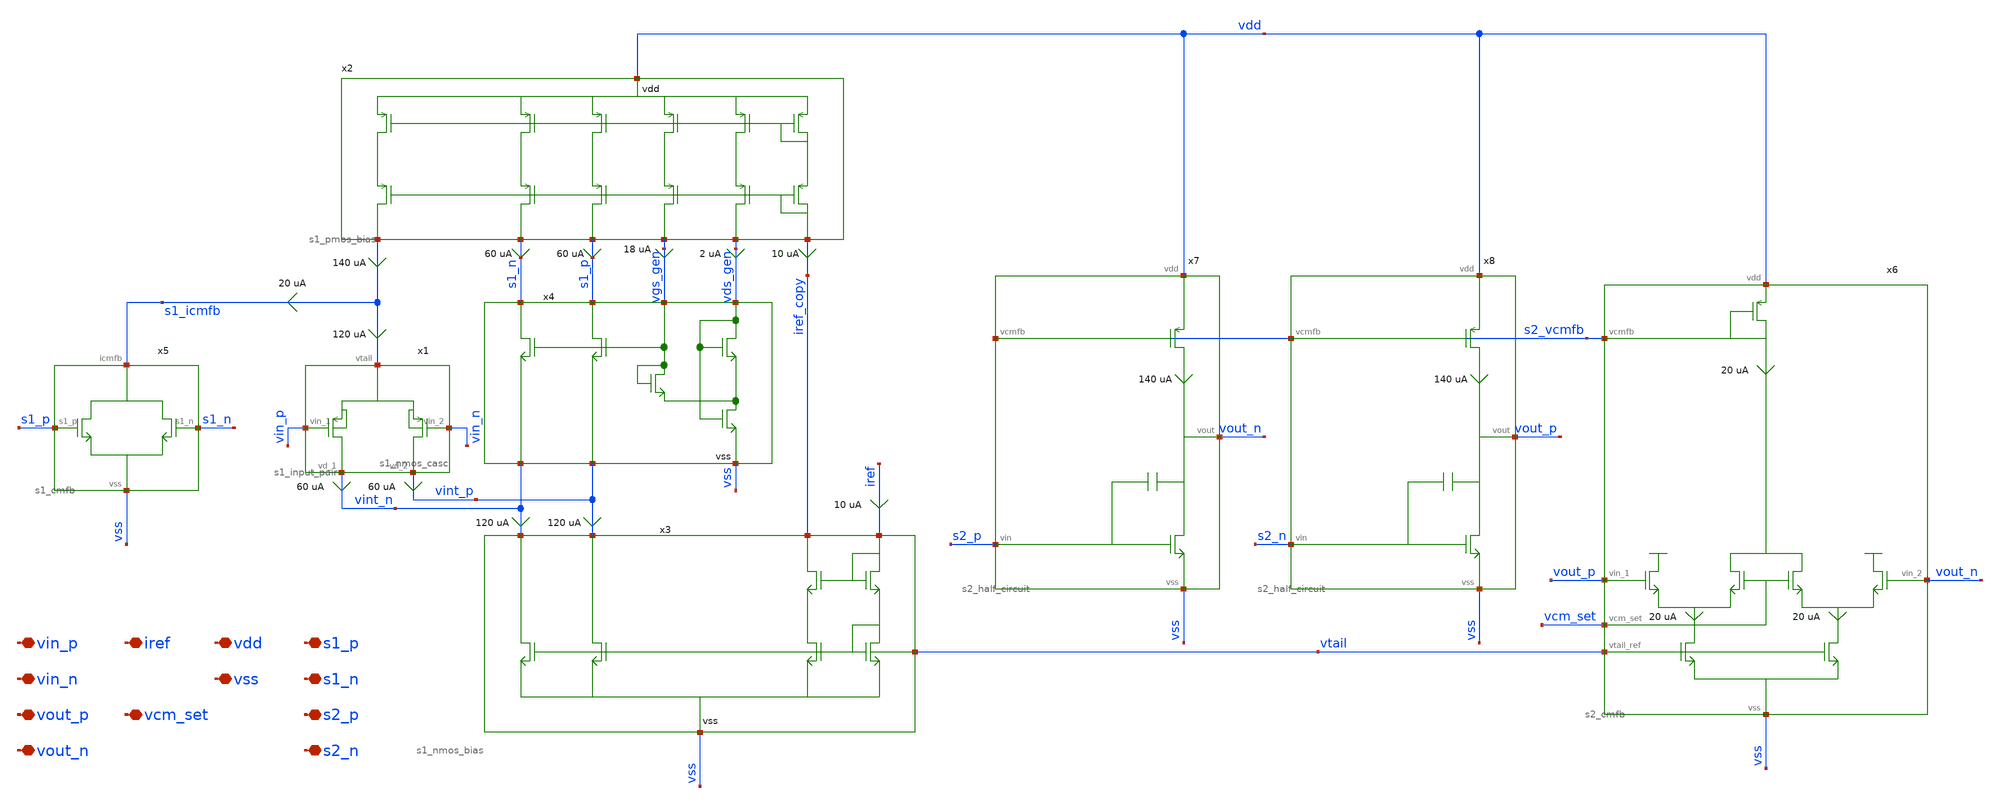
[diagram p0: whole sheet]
** sch_path: xschem/archive/ccia_top_level/ccia_main_ota.sch
**.subckt ccia_main_ota vin_p vin_n vout_p vout_n iref vdd vss vcm_set s1_p s1_n s2_p s2_n
*.iopin vin_p
*.iopin vin_n
*.iopin vout_p
*.iopin vout_n
*.iopin iref
*.iopin vdd
*.iopin vss
*.iopin vcm_set
*.iopin s1_p
*.iopin s1_n
*.iopin s2_p
*.iopin s2_n
x1 vint_n vint_p vin_p vin_n s1_icmfb s1_input_pair
x2 vdd s1_icmfb s1_n s1_p vgs_gen vds_gen iref_copy s1_pmos_bias
x3 iref iref_copy vint_n vint_p vss vtail s1_nmos_bias
x4 s1_n s1_p vint_n vint_p vgs_gen vds_gen vss s1_nmos_casc
x5 s1_icmfb s1_p s1_n vss s1_cmfb
x6 vout_p vout_n vcm_set vtail s2_vcmfb vdd vss s2_cmfb
x7 s2_vcmfb vdd vss s2_p vout_n s2_half_circuit
x8 s2_vcmfb vdd vss s2_n vout_p s2_half_circuit
**.ends
.end
